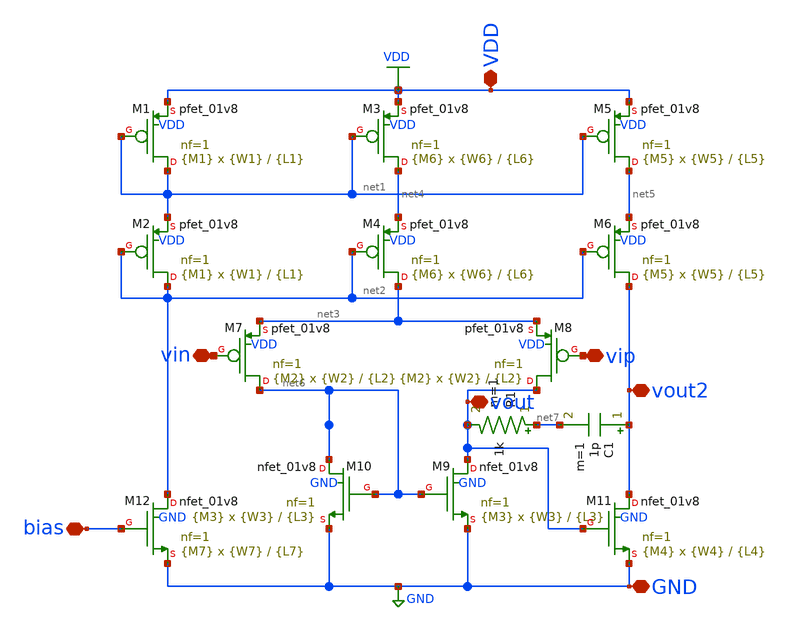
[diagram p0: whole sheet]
** sch_path: xschem/op6.sch
**.subckt op6 VDD GND vout vip vin vout2 bias
*.iopin VDD
*.iopin GND
*.iopin vout
*.iopin vip
*.iopin vin
*.iopin vout2
*.iopin bias
XM1 net1 net1 VDD VDD sky130_fd_pr__pfet_01v8 L={L1} W={W1} nf=1 ad='int((nf+1)/2) * W/nf * 0.29' as='int((nf+2)/2) * W/nf * 0.29'
+ pd='2*int((nf+1)/2) * (W/nf + 0.29)' ps='2*int((nf+2)/2) * (W/nf + 0.29)' nrd='0.29 / W' nrs='0.29 / W'
+ sa=0 sb=0 sd=0 mult={M1} m={M1}
XM2 net2 net2 net1 VDD sky130_fd_pr__pfet_01v8 L={L1} W={W1} nf=1 ad='int((nf+1)/2) * W/nf * 0.29' as='int((nf+2)/2) * W/nf * 0.29'
+ pd='2*int((nf+1)/2) * (W/nf + 0.29)' ps='2*int((nf+2)/2) * (W/nf + 0.29)' nrd='0.29 / W' nrs='0.29 / W'
+ sa=0 sb=0 sd=0 mult={M1} m={M1}
XM3 net4 net1 VDD VDD sky130_fd_pr__pfet_01v8 L={L6} W={W6} nf=1 ad='int((nf+1)/2) * W/nf * 0.29' as='int((nf+2)/2) * W/nf * 0.29'
+ pd='2*int((nf+1)/2) * (W/nf + 0.29)' ps='2*int((nf+2)/2) * (W/nf + 0.29)' nrd='0.29 / W' nrs='0.29 / W'
+ sa=0 sb=0 sd=0 mult={M6} m={M6}
XM4 net3 net2 net4 VDD sky130_fd_pr__pfet_01v8 L={L6} W={W6} nf=1 ad='int((nf+1)/2) * W/nf * 0.29' as='int((nf+2)/2) * W/nf * 0.29'
+ pd='2*int((nf+1)/2) * (W/nf + 0.29)' ps='2*int((nf+2)/2) * (W/nf + 0.29)' nrd='0.29 / W' nrs='0.29 / W'
+ sa=0 sb=0 sd=0 mult={M6} m={M6}
XM5 net5 net1 VDD VDD sky130_fd_pr__pfet_01v8 L={L5} W={W5} nf=1 ad='int((nf+1)/2) * W/nf * 0.29' as='int((nf+2)/2) * W/nf * 0.29'
+ pd='2*int((nf+1)/2) * (W/nf + 0.29)' ps='2*int((nf+2)/2) * (W/nf + 0.29)' nrd='0.29 / W' nrs='0.29 / W'
+ sa=0 sb=0 sd=0 mult={M5} m={M5}
XM6 vout2 net2 net5 VDD sky130_fd_pr__pfet_01v8 L={L5} W={W5} nf=1 ad='int((nf+1)/2) * W/nf * 0.29' as='int((nf+2)/2) * W/nf * 0.29'
+ pd='2*int((nf+1)/2) * (W/nf + 0.29)' ps='2*int((nf+2)/2) * (W/nf + 0.29)' nrd='0.29 / W' nrs='0.29 / W'
+ sa=0 sb=0 sd=0 mult={M5} m={M5}
XM7 net6 vin net3 VDD sky130_fd_pr__pfet_01v8 L={L2} W={W2} nf=1 ad='int((nf+1)/2) * W/nf * 0.29' as='int((nf+2)/2) * W/nf * 0.29'
+ pd='2*int((nf+1)/2) * (W/nf + 0.29)' ps='2*int((nf+2)/2) * (W/nf + 0.29)' nrd='0.29 / W' nrs='0.29 / W'
+ sa=0 sb=0 sd=0 mult={M2} m={M2}
XM8 vout vip net3 VDD sky130_fd_pr__pfet_01v8 L={L2} W={W2} nf=1 ad='int((nf+1)/2) * W/nf * 0.29' as='int((nf+2)/2) * W/nf * 0.29'
+ pd='2*int((nf+1)/2) * (W/nf + 0.29)' ps='2*int((nf+2)/2) * (W/nf + 0.29)' nrd='0.29 / W' nrs='0.29 / W'
+ sa=0 sb=0 sd=0 mult={M2} m={M2}
XM9 vout net6 GND GND sky130_fd_pr__nfet_01v8 L={L3} W={W3} nf=1 ad='int((nf+1)/2) * W/nf * 0.29' as='int((nf+2)/2) * W/nf * 0.29'
+ pd='2*int((nf+1)/2) * (W/nf + 0.29)' ps='2*int((nf+2)/2) * (W/nf + 0.29)' nrd='0.29 / W' nrs='0.29 / W'
+ sa=0 sb=0 sd=0 mult={M3} m={M3}
XM10 net6 net6 GND GND sky130_fd_pr__nfet_01v8 L={L3} W={W3} nf=1 ad='int((nf+1)/2) * W/nf * 0.29' as='int((nf+2)/2) * W/nf * 0.29'
+ pd='2*int((nf+1)/2) * (W/nf + 0.29)' ps='2*int((nf+2)/2) * (W/nf + 0.29)' nrd='0.29 / W' nrs='0.29 / W'
+ sa=0 sb=0 sd=0 mult={M3} m={M3}
XM11 vout2 vout GND GND sky130_fd_pr__nfet_01v8 L={L4} W={W4} nf=1 ad='int((nf+1)/2) * W/nf * 0.29' as='int((nf+2)/2) * W/nf * 0.29'
+ pd='2*int((nf+1)/2) * (W/nf + 0.29)' ps='2*int((nf+2)/2) * (W/nf + 0.29)' nrd='0.29 / W' nrs='0.29 / W'
+ sa=0 sb=0 sd=0 mult={M4} m={M4}
XM12 net2 bias GND GND sky130_fd_pr__nfet_01v8 L={L7} W={W7} nf=1 ad='int((nf+1)/2) * W/nf * 0.29' as='int((nf+2)/2) * W/nf * 0.29'
+ pd='2*int((nf+1)/2) * (W/nf + 0.29)' ps='2*int((nf+2)/2) * (W/nf + 0.29)' nrd='0.29 / W' nrs='0.29 / W'
+ sa=0 sb=0 sd=0 mult={M7} m={M7}
C1 vout2 net7 1p m=1
R1 net7 vout 1k m=1
**** begin user architecture code


***PMOS***
.param L1=1
.param W1=1
.param M1=4

***NMOS current source***
.param L7=1
.param W7=10
.param M7=4

***Diffpair***
.param L2=2.5
.param W2=35
.param M2=4

***NMOS load***
.param L3=2
.param W3=15
.param M3=4

***NMOS second stage***
.param L4=5
.param W4=30
.param M4=4

***PMOS current source second***
.param L5=0.4
.param W5=7
.param M5=4

***PMOS current source***
.param L6=0.4
.param W6=7
.param M6=4


**** end user architecture code
**.ends
.GLOBAL VDD
.GLOBAL GND
.end
